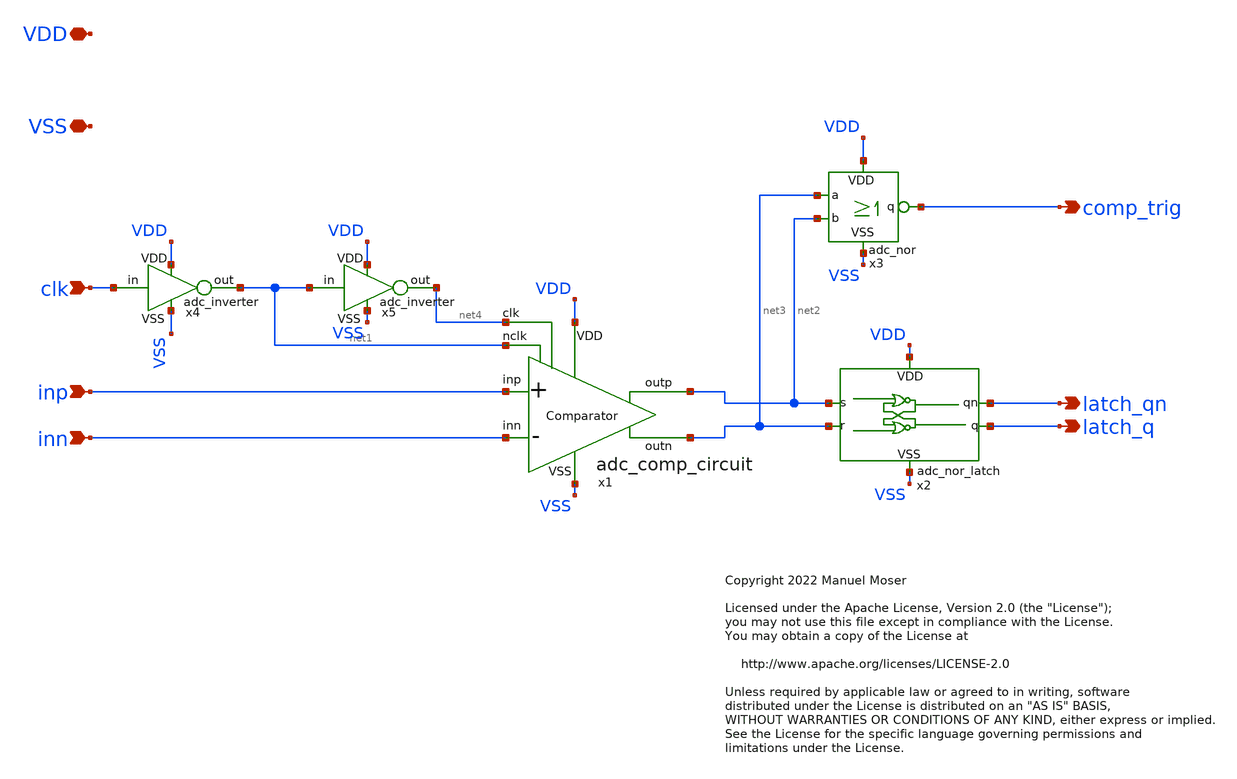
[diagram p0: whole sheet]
** sch_path: xschem/adc_comp_latch.sch
* Copyright 2022 Manuel Moser
* Licensed under the Apache License, Version 2.0 (the "License");
**.subckt adc_comp_latch VDD VSS clk inp inn comp_trig latch_qn latch_q
*.iopin VDD
*.iopin VSS
*.ipin clk
*.ipin inp
*.ipin inn
*.opin comp_trig
*.opin latch_qn
*.opin latch_q
x4 VDD VSS clk net1 adc_inverter
x5 VDD VSS net1 net4 adc_inverter
x1 VDD net4 net2 inp inn net3 net1 VSS adc_comp_circuit
x3 net2 net3 VDD comp_trig VSS adc_nor
x2 net2 latch_qn VDD latch_q VSS net3 adc_nor_latch
**.ends

* expanding   symbol:  adc_inverter.sym # of pins=4
** sym_path: xschem/adc_inverter.sym
** sch_path: xschem/adc_inverter.sch
.subckt adc_inverter VDD VSS in out
*.iopin VDD
*.iopin VSS
*.opin out
*.ipin in
XM1 out in VSS VSS sky130_fd_pr__nfet_01v8 L=0.15 W=0.42 nf=1 ad='int((nf+1)/2) * W/nf * 0.29' as='int((nf+2)/2) * W/nf * 0.29'
+ pd='2*int((nf+1)/2) * (W/nf + 0.29)' ps='2*int((nf+2)/2) * (W/nf + 0.29)' nrd='0.29 / W' nrs='0.29 / W'
+ sa=0 sb=0 sd=0 mult=1 m=1
XM2 out in VDD VDD sky130_fd_pr__pfet_01v8 L=0.15 W=0.84 nf=2 ad='int((nf+1)/2) * W/nf * 0.29' as='int((nf+2)/2) * W/nf * 0.29'
+ pd='2*int((nf+1)/2) * (W/nf + 0.29)' ps='2*int((nf+2)/2) * (W/nf + 0.29)' nrd='0.29 / W' nrs='0.29 / W'
+ sa=0 sb=0 sd=0 mult=1 m=1
.ends


* expanding   symbol:  adc_comp_circuit.sym # of pins=8
** sym_path: xschem/adc_comp_circuit.sym
** sch_path: xschem/adc_comp_circuit.sch
.subckt adc_comp_circuit VDD clk outp inp inn outn nclk VSS
*.iopin VDD
*.iopin VSS
*.ipin inp
*.ipin inn
*.ipin clk
*.ipin nclk
*.opin outp
*.opin outn
XM1 on clk VDD VDD sky130_fd_pr__pfet_01v8 L=0.15 W=2 nf=4 ad='int((nf+1)/2) * W/nf * 0.29' as='int((nf+2)/2) * W/nf * 0.29'
+ pd='2*int((nf+1)/2) * (W/nf + 0.29)' ps='2*int((nf+2)/2) * (W/nf + 0.29)' nrd='0.29 / W' nrs='0.29 / W'
+ sa=0 sb=0 sd=0 mult=1 m=1
XM2 op clk VDD VDD sky130_fd_pr__pfet_01v8 L=0.15 W=2 nf=4 ad='int((nf+1)/2) * W/nf * 0.29' as='int((nf+2)/2) * W/nf * 0.29'
+ pd='2*int((nf+1)/2) * (W/nf + 0.29)' ps='2*int((nf+2)/2) * (W/nf + 0.29)' nrd='0.29 / W' nrs='0.29 / W'
+ sa=0 sb=0 sd=0 mult=1 m=1
XM3 on inp net1 VSS sky130_fd_pr__nfet_01v8 L=0.15 W=8 nf=4 ad='int((nf+1)/2) * W/nf * 0.29' as='int((nf+2)/2) * W/nf * 0.29'
+ pd='2*int((nf+1)/2) * (W/nf + 0.29)' ps='2*int((nf+2)/2) * (W/nf + 0.29)' nrd='0.29 / W' nrs='0.29 / W'
+ sa=0 sb=0 sd=0 mult=1 m=1
XM4 op inn net1 VSS sky130_fd_pr__nfet_01v8 L=0.15 W=8 nf=4 ad='int((nf+1)/2) * W/nf * 0.29' as='int((nf+2)/2) * W/nf * 0.29'
+ pd='2*int((nf+1)/2) * (W/nf + 0.29)' ps='2*int((nf+2)/2) * (W/nf + 0.29)' nrd='0.29 / W' nrs='0.29 / W'
+ sa=0 sb=0 sd=0 mult=1 m=1
XM5 net1 clk VSS VSS sky130_fd_pr__nfet_01v8 L=0.15 W=4 nf=8 ad='int((nf+1)/2) * W/nf * 0.29' as='int((nf+2)/2) * W/nf * 0.29'
+ pd='2*int((nf+1)/2) * (W/nf + 0.29)' ps='2*int((nf+2)/2) * (W/nf + 0.29)' nrd='0.29 / W' nrs='0.29 / W'
+ sa=0 sb=0 sd=0 mult=1 m=1
XM6 net3 bp VDD VDD sky130_fd_pr__pfet_01v8 L=0.15 W=4 nf=2 ad='int((nf+1)/2) * W/nf * 0.29' as='int((nf+2)/2) * W/nf * 0.29'
+ pd='2*int((nf+1)/2) * (W/nf + 0.29)' ps='2*int((nf+2)/2) * (W/nf + 0.29)' nrd='0.29 / W' nrs='0.29 / W'
+ sa=0 sb=0 sd=0 mult=1 m=1
XM7 net2 bn VDD VDD sky130_fd_pr__pfet_01v8 L=0.15 W=4 nf=2 ad='int((nf+1)/2) * W/nf * 0.29' as='int((nf+2)/2) * W/nf * 0.29'
+ pd='2*int((nf+1)/2) * (W/nf + 0.29)' ps='2*int((nf+2)/2) * (W/nf + 0.29)' nrd='0.29 / W' nrs='0.29 / W'
+ sa=0 sb=0 sd=0 mult=1 m=1
XM8 bn op net3 VDD sky130_fd_pr__pfet_01v8 L=0.15 W=4 nf=2 ad='int((nf+1)/2) * W/nf * 0.29' as='int((nf+2)/2) * W/nf * 0.29'
+ pd='2*int((nf+1)/2) * (W/nf + 0.29)' ps='2*int((nf+2)/2) * (W/nf + 0.29)' nrd='0.29 / W' nrs='0.29 / W'
+ sa=0 sb=0 sd=0 mult=1 m=1
XM9 bp on net2 VDD sky130_fd_pr__pfet_01v8 L=0.15 W=4 nf=2 ad='int((nf+1)/2) * W/nf * 0.29' as='int((nf+2)/2) * W/nf * 0.29'
+ pd='2*int((nf+1)/2) * (W/nf + 0.29)' ps='2*int((nf+2)/2) * (W/nf + 0.29)' nrd='0.29 / W' nrs='0.29 / W'
+ sa=0 sb=0 sd=0 mult=1 m=1
XM10 bn bp VSS VSS sky130_fd_pr__nfet_01v8 L=0.15 W=2 nf=1 ad='int((nf+1)/2) * W/nf * 0.29' as='int((nf+2)/2) * W/nf * 0.29'
+ pd='2*int((nf+1)/2) * (W/nf + 0.29)' ps='2*int((nf+2)/2) * (W/nf + 0.29)' nrd='0.29 / W' nrs='0.29 / W'
+ sa=0 sb=0 sd=0 mult=1 m=1
XM11 bn nclk VSS VSS sky130_fd_pr__nfet_01v8 L=0.15 W=2 nf=1 ad='int((nf+1)/2) * W/nf * 0.29' as='int((nf+2)/2) * W/nf * 0.29'
+ pd='2*int((nf+1)/2) * (W/nf + 0.29)' ps='2*int((nf+2)/2) * (W/nf + 0.29)' nrd='0.29 / W' nrs='0.29 / W'
+ sa=0 sb=0 sd=0 mult=1 m=1
XM12 bp nclk VSS VSS sky130_fd_pr__nfet_01v8 L=0.15 W=2 nf=1 ad='int((nf+1)/2) * W/nf * 0.29' as='int((nf+2)/2) * W/nf * 0.29'
+ pd='2*int((nf+1)/2) * (W/nf + 0.29)' ps='2*int((nf+2)/2) * (W/nf + 0.29)' nrd='0.29 / W' nrs='0.29 / W'
+ sa=0 sb=0 sd=0 mult=1 m=1
XM13 bp bn VSS VSS sky130_fd_pr__nfet_01v8 L=0.15 W=2 nf=1 ad='int((nf+1)/2) * W/nf * 0.29' as='int((nf+2)/2) * W/nf * 0.29'
+ pd='2*int((nf+1)/2) * (W/nf + 0.29)' ps='2*int((nf+2)/2) * (W/nf + 0.29)' nrd='0.29 / W' nrs='0.29 / W'
+ sa=0 sb=0 sd=0 mult=1 m=1
x1 VDD VSS bp outp adc_comp_buffer
x2 VDD VSS bn outn adc_comp_buffer
x3 VSS VSS on VSS VSS adc_noise_decoup_cell2
x4 VSS VSS op VSS VSS adc_noise_decoup_cell2
.ends


* expanding   symbol:  adc_nor.sym # of pins=5
** sym_path: xschem/adc_nor.sym
** sch_path: xschem/adc_nor.sch
.subckt adc_nor b a VDD q VSS
*.iopin VDD
*.iopin VSS
*.ipin b
*.ipin a
*.opin q
XM5 q b VSS VSS sky130_fd_pr__nfet_01v8 L=0.15 W=0.42 nf=1 ad='int((nf+1)/2) * W/nf * 0.29' as='int((nf+2)/2) * W/nf * 0.29'
+ pd='2*int((nf+1)/2) * (W/nf + 0.29)' ps='2*int((nf+2)/2) * (W/nf + 0.29)' nrd='0.29 / W' nrs='0.29 / W'
+ sa=0 sb=0 sd=0 mult=1 m=1
XM6 q a VSS VSS sky130_fd_pr__nfet_01v8 L=0.15 W=0.42 nf=1 ad='int((nf+1)/2) * W/nf * 0.29' as='int((nf+2)/2) * W/nf * 0.29'
+ pd='2*int((nf+1)/2) * (W/nf + 0.29)' ps='2*int((nf+2)/2) * (W/nf + 0.29)' nrd='0.29 / W' nrs='0.29 / W'
+ sa=0 sb=0 sd=0 mult=1 m=1
XM1 q b net1 VDD sky130_fd_pr__pfet_01v8 L=0.15 W=0.8 nf=1 ad='int((nf+1)/2) * W/nf * 0.29' as='int((nf+2)/2) * W/nf * 0.29'
+ pd='2*int((nf+1)/2) * (W/nf + 0.29)' ps='2*int((nf+2)/2) * (W/nf + 0.29)' nrd='0.29 / W' nrs='0.29 / W'
+ sa=0 sb=0 sd=0 mult=1 m=1
XM2 q a net2 VDD sky130_fd_pr__pfet_01v8 L=0.15 W=0.8 nf=1 ad='int((nf+1)/2) * W/nf * 0.29' as='int((nf+2)/2) * W/nf * 0.29'
+ pd='2*int((nf+1)/2) * (W/nf + 0.29)' ps='2*int((nf+2)/2) * (W/nf + 0.29)' nrd='0.29 / W' nrs='0.29 / W'
+ sa=0 sb=0 sd=0 mult=1 m=1
XM3 net2 b VDD VDD sky130_fd_pr__pfet_01v8 L=0.15 W=0.8 nf=1 ad='int((nf+1)/2) * W/nf * 0.29' as='int((nf+2)/2) * W/nf * 0.29'
+ pd='2*int((nf+1)/2) * (W/nf + 0.29)' ps='2*int((nf+2)/2) * (W/nf + 0.29)' nrd='0.29 / W' nrs='0.29 / W'
+ sa=0 sb=0 sd=0 mult=1 m=1
XM4 net1 a VDD VDD sky130_fd_pr__pfet_01v8 L=0.15 W=0.8 nf=1 ad='int((nf+1)/2) * W/nf * 0.29' as='int((nf+2)/2) * W/nf * 0.29'
+ pd='2*int((nf+1)/2) * (W/nf + 0.29)' ps='2*int((nf+2)/2) * (W/nf + 0.29)' nrd='0.29 / W' nrs='0.29 / W'
+ sa=0 sb=0 sd=0 mult=1 m=1
.ends


* expanding   symbol:  adc_nor_latch.sym # of pins=6
** sym_path: xschem/adc_nor_latch.sym
** sch_path: xschem/adc_nor_latch.sch
.subckt adc_nor_latch s qn VDD q VSS r
*.iopin VDD
*.iopin VSS
*.ipin s
*.ipin r
*.opin q
*.opin qn
x1 q s VDD qn VSS adc_nor
x2 qn r VDD q VSS adc_nor
.ends


* expanding   symbol:  adc_comp_buffer.sym # of pins=4
** sym_path: xschem/adc_comp_buffer.sym
** sch_path: xschem/adc_comp_buffer.sch
.subckt adc_comp_buffer VDD VSS in out
*.iopin VDD
*.iopin VSS
*.ipin in
*.opin out
XM5 net1 in VSS VSS sky130_fd_pr__nfet_01v8 L=0.15 W=0.5 nf=1 ad='int((nf+1)/2) * W/nf * 0.29' as='int((nf+2)/2) * W/nf * 0.29'
+ pd='2*int((nf+1)/2) * (W/nf + 0.29)' ps='2*int((nf+2)/2) * (W/nf + 0.29)' nrd='0.29 / W' nrs='0.29 / W'
+ sa=0 sb=0 sd=0 mult=1 m=1
XM1 net1 in VDD VDD sky130_fd_pr__pfet_01v8 L=0.15 W=1 nf=1 ad='int((nf+1)/2) * W/nf * 0.29' as='int((nf+2)/2) * W/nf * 0.29'
+ pd='2*int((nf+1)/2) * (W/nf + 0.29)' ps='2*int((nf+2)/2) * (W/nf + 0.29)' nrd='0.29 / W' nrs='0.29 / W'
+ sa=0 sb=0 sd=0 mult=1 m=1
XM2 out net1 VDD VDD sky130_fd_pr__pfet_01v8 L=0.15 W=2 nf=2 ad='int((nf+1)/2) * W/nf * 0.29' as='int((nf+2)/2) * W/nf * 0.29'
+ pd='2*int((nf+1)/2) * (W/nf + 0.29)' ps='2*int((nf+2)/2) * (W/nf + 0.29)' nrd='0.29 / W' nrs='0.29 / W'
+ sa=0 sb=0 sd=0 mult=1 m=1
XM6 out net1 VSS VSS sky130_fd_pr__nfet_01v8 L=0.15 W=1 nf=2 ad='int((nf+1)/2) * W/nf * 0.29' as='int((nf+2)/2) * W/nf * 0.29'
+ pd='2*int((nf+1)/2) * (W/nf + 0.29)' ps='2*int((nf+2)/2) * (W/nf + 0.29)' nrd='0.29 / W' nrs='0.29 / W'
+ sa=0 sb=0 sd=0 mult=1 m=1
.ends


* expanding   symbol:  adc_noise_decoup_cell2.sym # of pins=5
** sym_path: xschem/adc_noise_decoup_cell2.sym
** sch_path: xschem/adc_noise_decoup_cell2.sch
.subckt adc_noise_decoup_cell2 mimcap_top mimcap_bot nmoscap_top nmoscap_bot pwell
*.iopin nmoscap_top
*.iopin mimcap_top
*.iopin mimcap_bot
*.iopin nmoscap_bot
*.iopin pwell
XC1 mimcap_top mimcap_bot sky130_fd_pr__cap_mim_m3_1 W=18.9 L=5.1 MF=1 m=1
XC2 nmoscap_top nmoscap_bot pwell sky130_fd_pr__cap_var_lvt W=18.4 L=3.9 VM=1 m=1
.ends

.end
